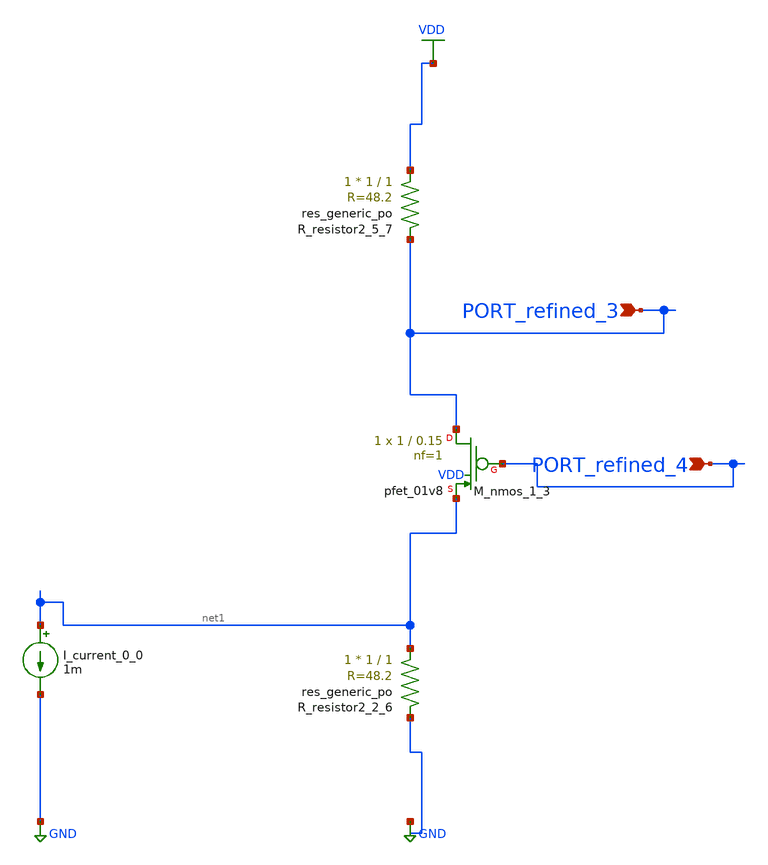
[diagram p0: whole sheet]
** sch_path: schematics/AMSNet/125.sch
**.subckt 125 PORT_refined_4 PORT_refined_3
*.ipin PORT_refined_4
*.ipin PORT_refined_3
I_current_0_0 net1 GND 1m
XM_nmos_1_3 PORT_refined_3 PORT_refined_4 net1 VDD sky130_fd_pr__pfet_01v8 L=0.15 W=1 nf=1 ad='int((1 + 1)/2) * 1 / 1 * 0.29'
+ as='int((1 + 2)/2) * 1 / 1 * 0.29' pd='2*int((1 + 1)/2) * (1 / 1 + 0.29)' ps='2*int((1 + 2)/2) * (1 / 1 + 0.29)'
+ nrd='0.29 / 1 ' nrs='0.29 / 1 ' sa=0 sb=0 sd=0 mult=1 m=1
XR_resistor2_2_6 net1 GND sky130_fd_pr__res_generic_po W=1 L=1 m=1
XR_resistor2_5_7 VDD PORT_refined_3 sky130_fd_pr__res_generic_po W=1 L=1 m=1
**.ends
.GLOBAL GND
.GLOBAL VDD
.end
